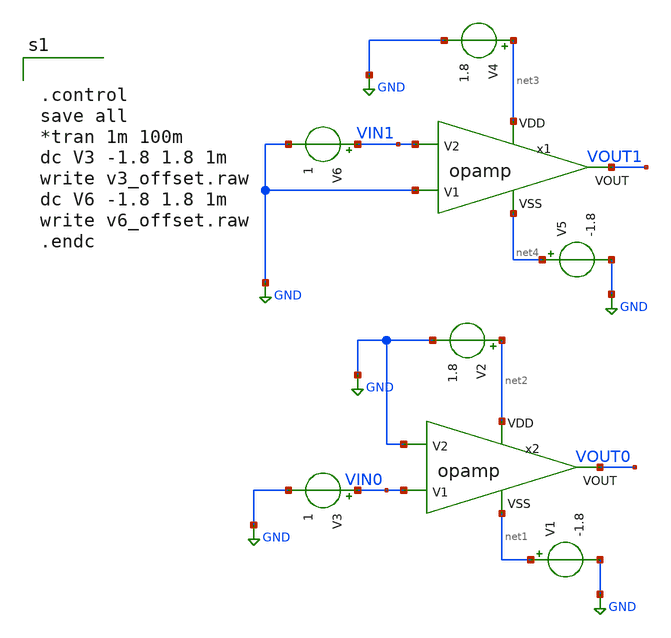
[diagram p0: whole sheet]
** sch_path: opamp_offset.sch
**.subckt opamp_offset
V2 net2 GND 1.8
V1 net1 GND -1.8
V3 VIN0 GND 1
V5 net4 GND -1.8
V6 VIN1 GND 1
V4 net3 GND 1.8
x1 net3 VIN1 GND VOUT1 net4 opamp
x2 net2 GND VIN0 VOUT0 net1 opamp
**** begin user architecture code


.control
save all
*tran 1m 100m
dc V3 -1.8 1.8 1m
write v3_offset.raw
dc V6 -1.8 1.8 1m
write v6_offset.raw
.endc



** opencircuitdesign pdks install
.lib $::SKYWATER_MODELS/sky130.lib.spice tt


**** end user architecture code
**.ends

* expanding   symbol:  /foss/designs/FINAL_PROJECT_KTMDT/opamp.sym # of pins=5
** sym_path: /foss/designs/FINAL_PROJECT_KTMDT/opamp.sym
** sch_path: /foss/designs/FINAL_PROJECT_KTMDT/opamp.sch
.subckt opamp VDD V2 V1 VOUT VSS
*.ipin VSS
*.ipin VDD
*.ipin V2
*.ipin V1
*.opin VOUT
XM3 net4 V2 net1 VSS sky130_fd_pr__nfet_g5v0d10v5 L=1 W=17.45 nf=1 ad='int((nf+1)/2) * W/nf * 0.29' as='int((nf+2)/2) * W/nf * 0.29'
+ pd='2*int((nf+1)/2) * (W/nf + 0.29)' ps='2*int((nf+2)/2) * (W/nf + 0.29)' nrd='0.29 / W' nrs='0.29 / W'
+ sa=0 sb=0 sd=0 mult=1 m=1
XM1 net5 net4 VDD VDD sky130_fd_pr__pfet_g5v0d10v5 L=1 W=30 nf=1 ad='int((nf+1)/2) * W/nf * 0.29' as='int((nf+2)/2) * W/nf * 0.29'
+ pd='2*int((nf+1)/2) * (W/nf + 0.29)' ps='2*int((nf+2)/2) * (W/nf + 0.29)' nrd='0.29 / W' nrs='0.29 / W'
+ sa=0 sb=0 sd=0 mult=1 m=1
XM4 net5 V1 net1 VSS sky130_fd_pr__nfet_g5v0d10v5 L=1 W=17.45 nf=1 ad='int((nf+1)/2) * W/nf * 0.29' as='int((nf+2)/2) * W/nf * 0.29'
+ pd='2*int((nf+1)/2) * (W/nf + 0.29)' ps='2*int((nf+2)/2) * (W/nf + 0.29)' nrd='0.29 / W' nrs='0.29 / W'
+ sa=0 sb=0 sd=0 mult=1 m=1
XM6 net1 net6 VSS VSS sky130_fd_pr__nfet_g5v0d10v5 L=1 W=15.17 nf=1 ad='int((nf+1)/2) * W/nf * 0.29'
+ as='int((nf+2)/2) * W/nf * 0.29' pd='2*int((nf+1)/2) * (W/nf + 0.29)' ps='2*int((nf+2)/2) * (W/nf + 0.29)'
+ nrd='0.29 / W' nrs='0.29 / W' sa=0 sb=0 sd=0 mult=1 m=1
XM7 VOUT net6 VSS VSS sky130_fd_pr__nfet_g5v0d10v5 L=1 W=19 nf=1 ad='int((nf+1)/2) * W/nf * 0.29' as='int((nf+2)/2) * W/nf * 0.29'
+ pd='2*int((nf+1)/2) * (W/nf + 0.29)' ps='2*int((nf+2)/2) * (W/nf + 0.29)' nrd='0.29 / W' nrs='0.29 / W'
+ sa=0 sb=0 sd=0 mult=1 m=1
XM5 net6 net6 VSS VSS sky130_fd_pr__nfet_g5v0d10v5 L=1 W=15.17 nf=1 ad='int((nf+1)/2) * W/nf * 0.29'
+ as='int((nf+2)/2) * W/nf * 0.29' pd='2*int((nf+1)/2) * (W/nf + 0.29)' ps='2*int((nf+2)/2) * (W/nf + 0.29)'
+ nrd='0.29 / W' nrs='0.29 / W' sa=0 sb=0 sd=0 mult=1 m=1
XM2 net4 net4 VDD VDD sky130_fd_pr__pfet_g5v0d10v5 L=1 W=30 nf=1 ad='int((nf+1)/2) * W/nf * 0.29' as='int((nf+2)/2) * W/nf * 0.29'
+ pd='2*int((nf+1)/2) * (W/nf + 0.29)' ps='2*int((nf+2)/2) * (W/nf + 0.29)' nrd='0.29 / W' nrs='0.29 / W'
+ sa=0 sb=0 sd=0 mult=1 m=1
XM8 VOUT net5 VDD VDD sky130_fd_pr__pfet_g5v0d10v5 L=1 W=38 nf=1 ad='int((nf+1)/2) * W/nf * 0.29' as='int((nf+2)/2) * W/nf * 0.29'
+ pd='2*int((nf+1)/2) * (W/nf + 0.29)' ps='2*int((nf+2)/2) * (W/nf + 0.29)' nrd='0.29 / W' nrs='0.29 / W'
+ sa=0 sb=0 sd=0 mult=2 m=2
V_ibias net7 net6 0
.save i(v_ibias)
XR1 net2 VDD VSS sky130_fd_pr__res_high_po W=1 L=41.1 mult=1 m=1
XR2 net3 net2 VSS sky130_fd_pr__res_high_po W=1 L=41.1 mult=1 m=1
XR3 net7 net3 VSS sky130_fd_pr__res_high_po W=1 L=41.1 mult=1 m=1
XR4 net8 VOUT VSS sky130_fd_pr__res_high_po W=1 L=5 mult=1 m=1
XC1 net8 net5 sky130_fd_pr__cap_mim_m3_1 W=9 L=9 MF=2 m=2
.ends

.GLOBAL GND
.end
